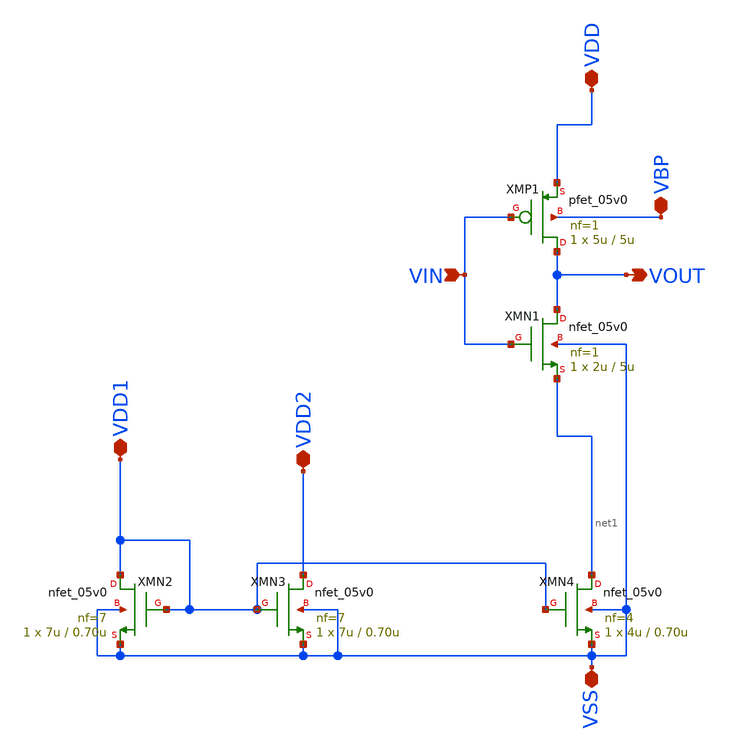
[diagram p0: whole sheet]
** sch_path: xschem/vco/vco_inv-nmosmirr_forlvs.sch
**.subckt vco_inv-nmosmirr_forlvs VSS VDD1 VDD2 VDD VIN VOUT VBP
*.iopin VSS
*.iopin VDD1
*.iopin VDD2
*.iopin VDD
*.ipin VIN
*.opin VOUT
*.iopin VBP
XMN2 VDD1 VDD1 VSS VSS nfet_05v0 L=0.70u W=7u nf=7 ad='int((nf+1)/2) * W/nf * 0.18u' as='int((nf+2)/2) * W/nf * 0.18u'
+ pd='2*int((nf+1)/2) * (W/nf + 0.18u)' ps='2*int((nf+2)/2) * (W/nf + 0.18u)' nrd='0.18u / W' nrs='0.18u / W'
+ sa=0 sb=0 sd=0 m=1
XMN3 VDD2 VDD1 VSS VSS nfet_05v0 L=0.70u W=7u nf=7 ad='int((nf+1)/2) * W/nf * 0.18u' as='int((nf+2)/2) * W/nf * 0.18u'
+ pd='2*int((nf+1)/2) * (W/nf + 0.18u)' ps='2*int((nf+2)/2) * (W/nf + 0.18u)' nrd='0.18u / W' nrs='0.18u / W'
+ sa=0 sb=0 sd=0 m=1
XMN4 net1 VDD1 VSS VSS nfet_05v0 L=0.70u W=4u nf=4 ad='int((nf+1)/2) * W/nf * 0.18u' as='int((nf+2)/2) * W/nf * 0.18u'
+ pd='2*int((nf+1)/2) * (W/nf + 0.18u)' ps='2*int((nf+2)/2) * (W/nf + 0.18u)' nrd='0.18u / W' nrs='0.18u / W'
+ sa=0 sb=0 sd=0 m=1
XMN1 VOUT VIN net1 VSS nfet_05v0 L=5u W=2u nf=1 ad='int((nf+1)/2) * W/nf * 0.18u' as='int((nf+2)/2) * W/nf * 0.18u'
+ pd='2*int((nf+1)/2) * (W/nf + 0.18u)' ps='2*int((nf+2)/2) * (W/nf + 0.18u)' nrd='0.18u / W' nrs='0.18u / W'
+ sa=0 sb=0 sd=0 m=1
XMP1 VOUT VIN VDD VBP pfet_05v0 L=5u W=5u nf=1 ad='int((nf+1)/2) * W/nf * 0.18u' as='int((nf+2)/2) * W/nf * 0.18u'
+ pd='2*int((nf+1)/2) * (W/nf + 0.18u)' ps='2*int((nf+2)/2) * (W/nf + 0.18u)' nrd='0.18u / W' nrs='0.18u / W'
+ sa=0 sb=0 sd=0 m=1
**.ends
.end
